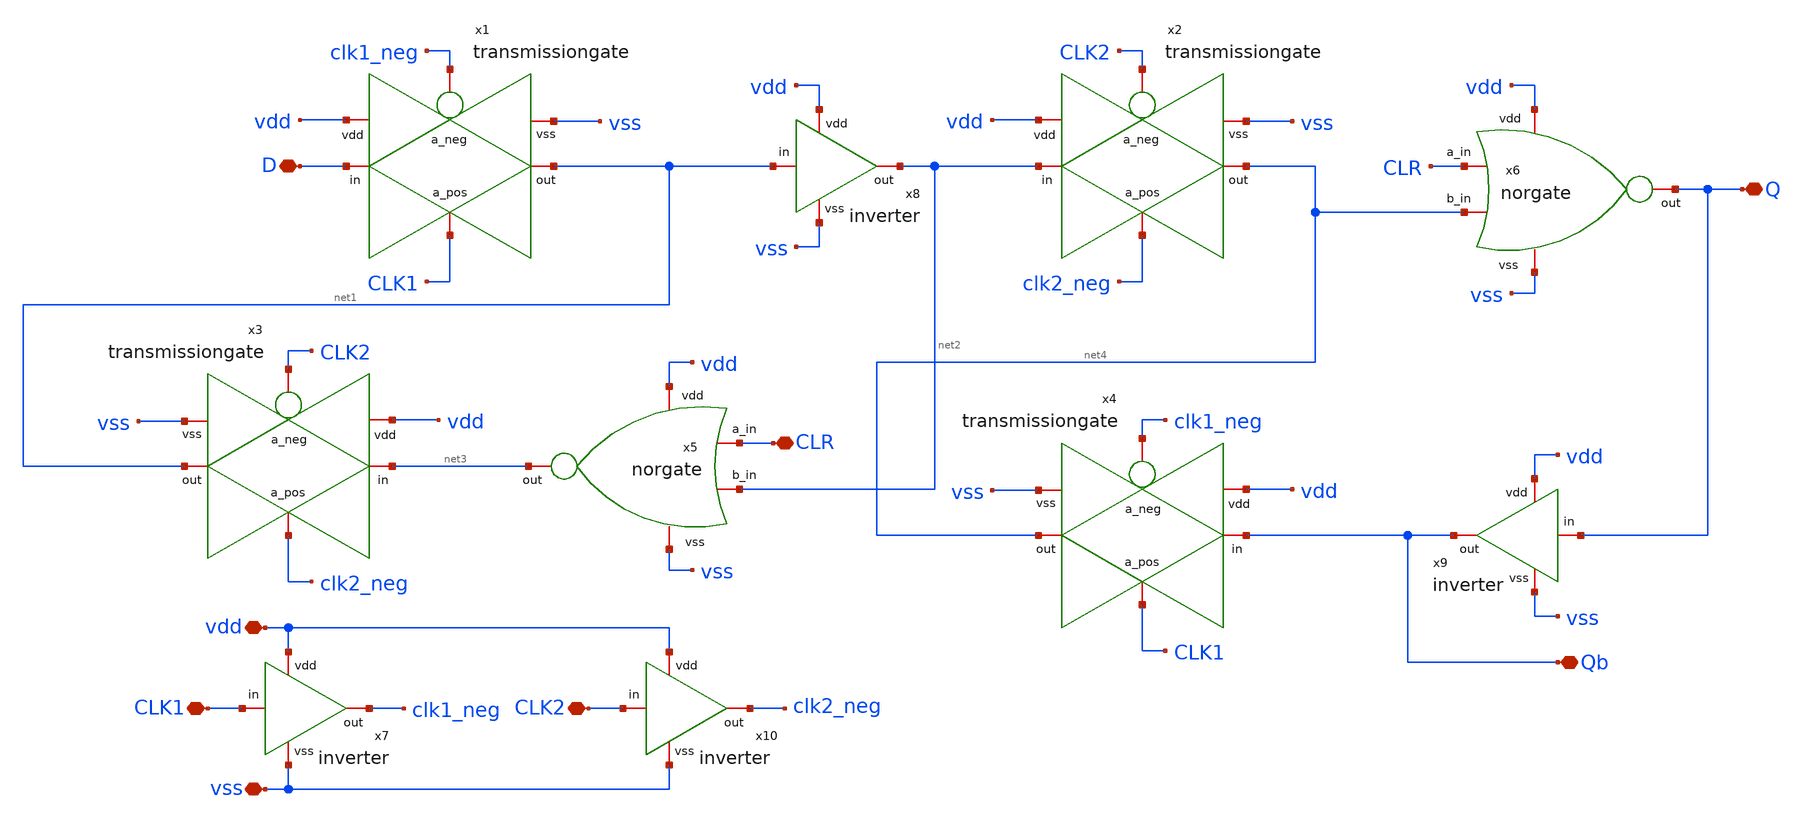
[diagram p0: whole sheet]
** sch_path: design/blocks/dff2c/schematic/dff2c.sch
**.subckt dff2c D Q Qb CLK1 CLR vdd vss CLK2
*.iopin D
*.iopin Q
*.iopin Qb
*.iopin CLK1
*.iopin CLR
*.iopin vdd
*.iopin vss
*.iopin CLK2
x1 clk1_neg net1 D vdd vss CLK1 transmissiongate
x2 CLK2 net4 net2 vdd vss clk2_neg transmissiongate
x3 CLK2 net1 net3 vdd vss clk2_neg transmissiongate
x4 clk1_neg net4 Qb vdd vss CLK1 transmissiongate
x5 vdd net2 CLR net3 vss norgate
x6 vdd net4 CLR Q vss norgate
x7 vdd clk1_neg CLK1 vss inverter
x8 vdd net2 net1 vss inverter
x9 vdd Qb Q vss inverter
x10 vdd clk2_neg CLK2 vss inverter
**.ends

* expanding   symbol:  blocks/transmissiongate/schematic/transmissiongate.sym # of pins=6
** sym_path: design/blocks/transmissiongate/schematic/transmissiongate.sym
** sch_path: design/blocks/transmissiongate/schematic/transmissiongate.sch
.subckt transmissiongate a_neg out in vdd vss a_pos
*.iopin vdd
*.iopin vss
*.iopin out
*.iopin in
*.iopin a_neg
*.iopin a_pos
XM0 in a_neg out vdd sky130_fd_pr__pfet_01v8 L=0.15 W=1.5 nf=1 ad='int((nf+1)/2) * W/nf * 0.29' as='int((nf+2)/2) * W/nf * 0.29'
+ pd='2*int((nf+1)/2) * (W/nf + 0.29)' ps='2*int((nf+2)/2) * (W/nf + 0.29)' nrd='0.29 / W' nrs='0.29 / W'
+ sa=0 sb=0 sd=0 mult=1 m=1
XM1 out a_pos in vss sky130_fd_pr__nfet_01v8 L=0.15 W=0.75 nf=1 ad='int((nf+1)/2) * W/nf * 0.29' as='int((nf+2)/2) * W/nf * 0.29'
+ pd='2*int((nf+1)/2) * (W/nf + 0.29)' ps='2*int((nf+2)/2) * (W/nf + 0.29)' nrd='0.29 / W' nrs='0.29 / W'
+ sa=0 sb=0 sd=0 mult=1 m=1
.ends


* expanding   symbol:  blocks/norgate/schematic/norgate.sym # of pins=5
** sym_path: design/blocks/norgate/schematic/norgate.sym
** sch_path: design/blocks/norgate/schematic/norgate.sch
.subckt norgate vdd b_in a_in out vss
*.iopin a_in
*.iopin out
*.iopin vss
*.iopin vdd
*.iopin b_in
XM1 net1 b_in vdd vdd sky130_fd_pr__pfet_01v8 L=0.15 W=3 nf=1 ad='int((nf+1)/2) * W/nf * 0.29' as='int((nf+2)/2) * W/nf * 0.29'
+ pd='2*int((nf+1)/2) * (W/nf + 0.29)' ps='2*int((nf+2)/2) * (W/nf + 0.29)' nrd='0.29 / W' nrs='0.29 / W'
+ sa=0 sb=0 sd=0 mult=1 m=1
XM2 out a_in vss vss sky130_fd_pr__nfet_01v8 L=0.15 W=0.75 nf=1 ad='int((nf+1)/2) * W/nf * 0.29' as='int((nf+2)/2) * W/nf * 0.29'
+ pd='2*int((nf+1)/2) * (W/nf + 0.29)' ps='2*int((nf+2)/2) * (W/nf + 0.29)' nrd='0.29 / W' nrs='0.29 / W'
+ sa=0 sb=0 sd=0 mult=1 m=1
XM3 out b_in vss vss sky130_fd_pr__nfet_01v8 L=0.15 W=0.75 nf=1 ad='int((nf+1)/2) * W/nf * 0.29' as='int((nf+2)/2) * W/nf * 0.29'
+ pd='2*int((nf+1)/2) * (W/nf + 0.29)' ps='2*int((nf+2)/2) * (W/nf + 0.29)' nrd='0.29 / W' nrs='0.29 / W'
+ sa=0 sb=0 sd=0 mult=1 m=1
XM4 out a_in net1 vdd sky130_fd_pr__pfet_01v8 L=0.15 W=3 nf=1 ad='int((nf+1)/2) * W/nf * 0.29' as='int((nf+2)/2) * W/nf * 0.29'
+ pd='2*int((nf+1)/2) * (W/nf + 0.29)' ps='2*int((nf+2)/2) * (W/nf + 0.29)' nrd='0.29 / W' nrs='0.29 / W'
+ sa=0 sb=0 sd=0 mult=1 m=1
.ends


* expanding   symbol:  blocks/inverter/schematic/inverter.sym # of pins=4
** sym_path: design/blocks/inverter/schematic/inverter.sym
** sch_path: design/blocks/inverter/schematic/inverter.sch
.subckt inverter vdd out in vss
*.iopin vdd
*.iopin out
*.iopin vss
*.iopin in
XM1 out in vss vss sky130_fd_pr__nfet_01v8 L=0.15 W=0.75 nf=1 ad='int((nf+1)/2) * W/nf * 0.29' as='int((nf+2)/2) * W/nf * 0.29'
+ pd='2*int((nf+1)/2) * (W/nf + 0.29)' ps='2*int((nf+2)/2) * (W/nf + 0.29)' nrd='0.29 / W' nrs='0.29 / W'
+ sa=0 sb=0 sd=0 mult=1 m=1
XM2 out in vdd vdd sky130_fd_pr__pfet_01v8 L=0.15 W=1.5 nf=1 ad='int((nf+1)/2) * W/nf * 0.29' as='int((nf+2)/2) * W/nf * 0.29'
+ pd='2*int((nf+1)/2) * (W/nf + 0.29)' ps='2*int((nf+2)/2) * (W/nf + 0.29)' nrd='0.29 / W' nrs='0.29 / W'
+ sa=0 sb=0 sd=0 mult=1 m=1
.ends

.end
